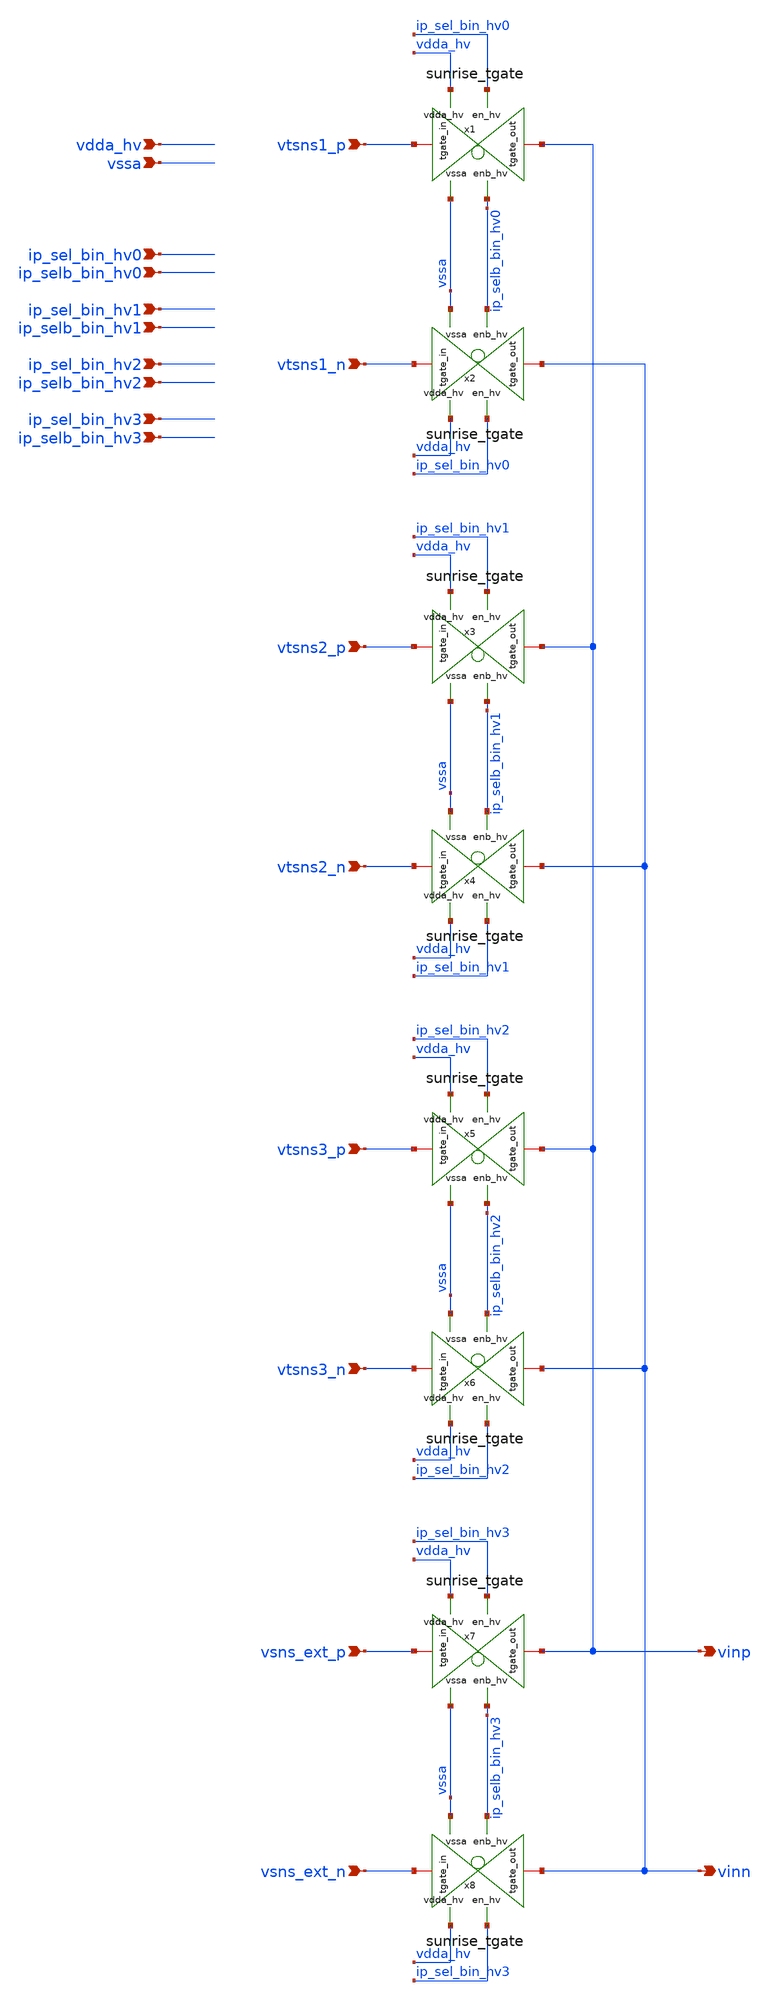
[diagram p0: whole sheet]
** sch_path: Schematics_Layout/sunrise_mux/sunrise_mux.sch
**.subckt sunrise_mux ip_sel_bin_hv0 ip_selb_bin_hv0 vsns_ext_p vsns_ext_n vtsns1_p vtsns1_n vdda_hv
*+ vssa vtsns2_p vtsns2_n vtsns3_p vtsns3_n ip_sel_bin_hv1 ip_selb_bin_hv1 ip_sel_bin_hv2 ip_selb_bin_hv2
*+ ip_sel_bin_hv3 ip_selb_bin_hv3 vinp vinn
*.ipin ip_sel_bin_hv0
*.ipin ip_selb_bin_hv0
*.ipin vsns_ext_p
*.ipin vsns_ext_n
*.ipin vtsns1_p
*.ipin vtsns1_n
*.ipin vdda_hv
*.ipin vssa
*.ipin vtsns2_p
*.ipin vtsns2_n
*.ipin vtsns3_p
*.ipin vtsns3_n
*.ipin ip_sel_bin_hv1
*.ipin ip_selb_bin_hv1
*.ipin ip_sel_bin_hv2
*.ipin ip_selb_bin_hv2
*.ipin ip_sel_bin_hv3
*.ipin ip_selb_bin_hv3
*.opin vinp
*.opin vinn
x1 vdda_hv vssa ip_sel_bin_hv0 vtsns1_p vinp ip_selb_bin_hv0 sunrise_tgate
x2 vdda_hv vssa ip_sel_bin_hv0 vtsns1_n vinn ip_selb_bin_hv0 sunrise_tgate
x3 vdda_hv vssa ip_sel_bin_hv1 vtsns2_p vinp ip_selb_bin_hv1 sunrise_tgate
x4 vdda_hv vssa ip_sel_bin_hv1 vtsns2_n vinn ip_selb_bin_hv1 sunrise_tgate
x5 vdda_hv vssa ip_sel_bin_hv2 vtsns3_p vinp ip_selb_bin_hv2 sunrise_tgate
x6 vdda_hv vssa ip_sel_bin_hv2 vtsns3_n vinn ip_selb_bin_hv2 sunrise_tgate
x7 vdda_hv vssa ip_sel_bin_hv3 vsns_ext_p vinp ip_selb_bin_hv3 sunrise_tgate
x8 vdda_hv vssa ip_sel_bin_hv3 vsns_ext_n vinn ip_selb_bin_hv3 sunrise_tgate
**.ends
.end
